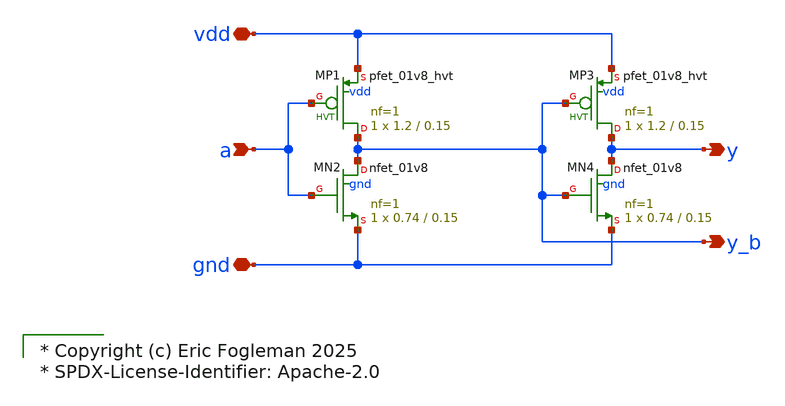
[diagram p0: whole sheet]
** sch_path: xschem/ejf_pll96_dbuf.sch

* Copyright (c) Eric Fogleman 2025
* SPDX-License-Identifier: Apache-2.0

**.subckt ejf_pll96_dbuf a vdd gnd y y_b
*.ipin a
*.iopin vdd
*.iopin gnd
*.opin y
*.opin y_b
XMP1 y_b a vdd vdd sky130_fd_pr__pfet_01v8_hvt L=0.15 W=1.2 nf=1 ad='int((nf+1)/2) * W/nf * 0.29' as='int((nf+2)/2) * W/nf * 0.29'
+ pd='2*int((nf+1)/2) * (W/nf + 0.29)' ps='2*int((nf+2)/2) * (W/nf + 0.29)' nrd='0.29 / W' nrs='0.29 / W'
+ sa=0 sb=0 sd=0 mult=1 m=1
XMP3 y y_b vdd vdd sky130_fd_pr__pfet_01v8_hvt L=0.15 W=1.2 nf=1 ad='int((nf+1)/2) * W/nf * 0.29' as='int((nf+2)/2) * W/nf * 0.29'
+ pd='2*int((nf+1)/2) * (W/nf + 0.29)' ps='2*int((nf+2)/2) * (W/nf + 0.29)' nrd='0.29 / W' nrs='0.29 / W'
+ sa=0 sb=0 sd=0 mult=1 m=1
XMN4 y y_b gnd gnd sky130_fd_pr__nfet_01v8 L=0.15 W=0.74 nf=1 ad='int((nf+1)/2) * W/nf * 0.29' as='int((nf+2)/2) * W/nf * 0.29'
+ pd='2*int((nf+1)/2) * (W/nf + 0.29)' ps='2*int((nf+2)/2) * (W/nf + 0.29)' nrd='0.29 / W' nrs='0.29 / W'
+ sa=0 sb=0 sd=0 mult=1 m=1
XMN2 y_b a gnd gnd sky130_fd_pr__nfet_01v8 L=0.15 W=0.74 nf=1 ad='int((nf+1)/2) * W/nf * 0.29' as='int((nf+2)/2) * W/nf * 0.29'
+ pd='2*int((nf+1)/2) * (W/nf + 0.29)' ps='2*int((nf+2)/2) * (W/nf + 0.29)' nrd='0.29 / W' nrs='0.29 / W'
+ sa=0 sb=0 sd=0 mult=1 m=1
**.ends
.end
